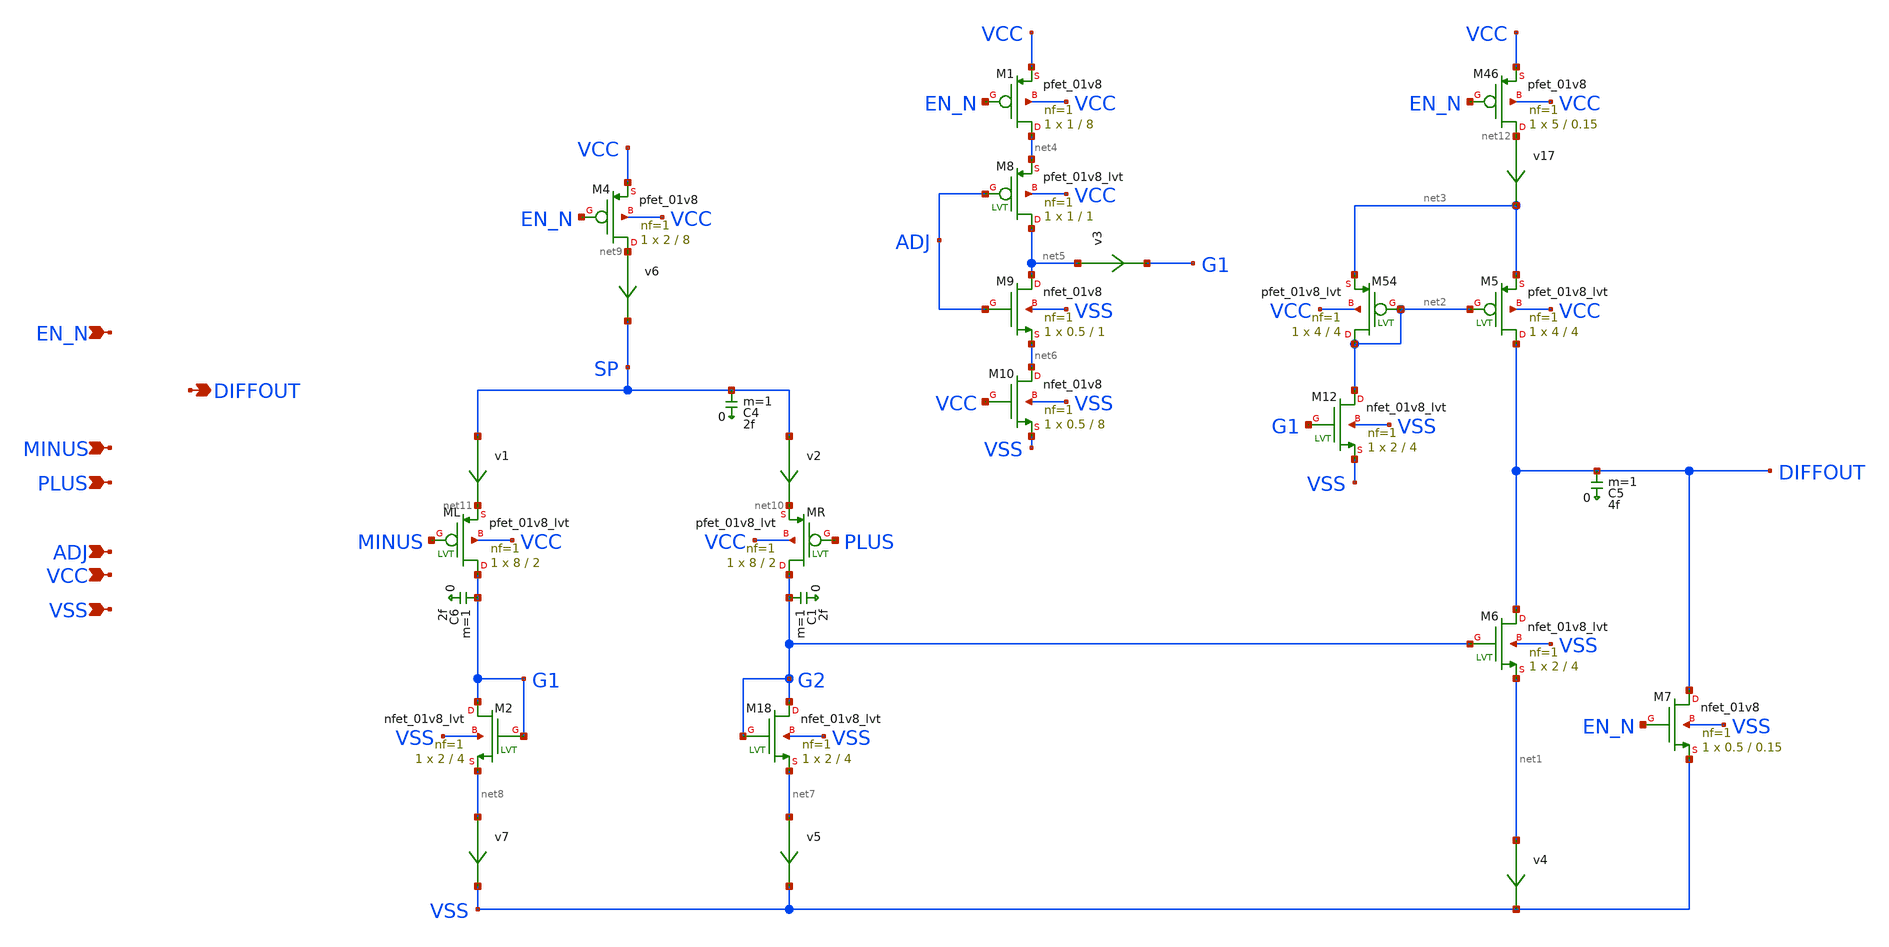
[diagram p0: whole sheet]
** sch_path: sky130A/xschem_libs/sky130_tests/zero_opamp/schematic/zero_opamp.sch
* Copyright 2021 Stefan Frederik Schippers
* Licensed under the Apache License, Version 2.0 (the "License");
* you may not use this file except in compliance with the License.
* You may obtain a copy of the License at
* https://www.apache.org/licenses/LICENSE-2.0
* Unless required by applicable law or agreed to in writing, software
* distributed under the License is distributed on an "AS IS" BASIS,
* WITHOUT WARRANTIES OR CONDITIONS OF ANY KIND, either express or implied.
* See the License for the specific language governing permissions and
* limitations under the License.
**.subckt zero_opamp PLUS MINUS EN_N VSS VCC DIFFOUT ADJ
*.ipin PLUS
*.ipin MINUS
*.ipin EN_N
*.ipin VSS
*.ipin VCC
*.opin DIFFOUT
*.ipin ADJ
C6 G1 0 2f m=1
XM4 net9 EN_N VCC VCC sky130_fd_pr__pfet_01v8 L=8 W=2 nf=1 ad='int((nf+1)/2) * W/nf * 0.29' as='int((nf+2)/2) * W/nf * 0.29'
+ pd='2*int((nf+1)/2) * (W/nf + 0.29)' ps='2*int((nf+2)/2) * (W/nf + 0.29)' nrd='0.29 / W' nrs='0.29 / W'
+ sa=0 sb=0 sd=0 mult=1 m=1
XM18 G2 G2 net7 VSS sky130_fd_pr__nfet_01v8_lvt L=4 W=2 nf=1 ad='int((1 + 1)/2) * 2 / 1 * 0.29' as='int((1 + 2)/2) * 2 / 1 * 0.29'
+ pd='2*int((1 + 1)/2) * (2 / 1 + 0.29)' ps='2*int((1 + 2)/2) * (2 / 1 + 0.29)' nrd='0.29 / 2 ' nrs='0.29 / 2 '
+ sa=0 sb=0 sd=0 mult=1 m=1
XM2 G1 G1 net8 VSS sky130_fd_pr__nfet_01v8_lvt L=4 W=2 nf=1 ad='int((1 + 1)/2) * 2 / 1 * 0.29' as='int((1 + 2)/2) * 2 / 1 * 0.29'
+ pd='2*int((1 + 1)/2) * (2 / 1 + 0.29)' ps='2*int((1 + 2)/2) * (2 / 1 + 0.29)' nrd='0.29 / 2 ' nrs='0.29 / 2 '
+ sa=0 sb=0 sd=0 mult=1 m=1
XMR G2 PLUS net10 VCC sky130_fd_pr__pfet_01v8_lvt L=2 W=8 nf=1 ad='int((1 + 1)/2) * 8 / 1 * 0.29' as='int((1 + 2)/2) * 8 / 1 * 0.29'
+ pd='2*int((1 + 1)/2) * (8 / 1 + 0.29)' ps='2*int((1 + 2)/2) * (8 / 1 + 0.29)' nrd='0.29 / 8 ' nrs='0.29 / 8 '
+ sa=0 sb=0 sd=0 mult=1 m=1
XML G1 MINUS net11 VCC sky130_fd_pr__pfet_01v8_lvt L=2 W=8 nf=1 ad='int((1 + 1)/2) * 8 / 1 * 0.29' as='int((1 + 2)/2) * 8 / 1 * 0.29'
+ pd='2*int((1 + 1)/2) * (8 / 1 + 0.29)' ps='2*int((1 + 2)/2) * (8 / 1 + 0.29)' nrd='0.29 / 8 ' nrs='0.29 / 8 '
+ sa=0 sb=0 sd=0 mult=1 m=1
v1 SP net11 0
.save i(v1)
C4 SP 0 2f m=1
C1 G2 0 2f m=1
C5 DIFFOUT 0 4f m=1
XM6 DIFFOUT G2 net1 VSS sky130_fd_pr__nfet_01v8_lvt L=4 W=2 nf=1 ad='int((1 + 1)/2) * 2 / 1 * 0.29' as='int((1 + 2)/2) * 2 / 1 * 0.29'
+ pd='2*int((1 + 1)/2) * (2 / 1 + 0.29)' ps='2*int((1 + 2)/2) * (2 / 1 + 0.29)' nrd='0.29 / 2 ' nrs='0.29 / 2 '
+ sa=0 sb=0 sd=0 mult=1 m=1
v2 SP net10 0
.save i(v2)
v4 net1 VSS 0
.save i(v4)
v6 net9 SP 0
.save i(v6)
XM7 DIFFOUT EN_N VSS VSS sky130_fd_pr__nfet_01v8 L=0.15 W=0.5 nf=1 ad='int((1 + 1)/2) * 0.5 / 1 * 0.29'
+ as='int((1 + 2)/2) * 0.5 / 1 * 0.29' pd='2*int((1 + 1)/2) * (0.5 / 1 + 0.29)' ps='2*int((1 + 2)/2) * (0.5 / 1 + 0.29)'
+ nrd='0.29 / 0.5 ' nrs='0.29 / 0.5 ' sa=0 sb=0 sd=0 mult=1 m=1
XM46 net12 EN_N VCC VCC sky130_fd_pr__pfet_01v8 L=0.15 W=5 nf=1 ad='int((nf+1)/2) * W/nf * 0.29' as='int((nf+2)/2) * W/nf * 0.29'
+ pd='2*int((nf+1)/2) * (W/nf + 0.29)' ps='2*int((nf+2)/2) * (W/nf + 0.29)' nrd='0.29 / W' nrs='0.29 / W'
+ sa=0 sb=0 sd=0 mult=1 m=1
v17 net12 net3 0
.save i(v17)
XM12 net2 G1 VSS VSS sky130_fd_pr__nfet_01v8_lvt L=4 W=2 nf=1 ad='int((1 + 1)/2) * 2 / 1 * 0.29' as='int((1 + 2)/2) * 2 / 1 * 0.29'
+ pd='2*int((1 + 1)/2) * (2 / 1 + 0.29)' ps='2*int((1 + 2)/2) * (2 / 1 + 0.29)' nrd='0.29 / 2 ' nrs='0.29 / 2 '
+ sa=0 sb=0 sd=0 mult=1 m=1
XM54 net2 net2 net3 VCC sky130_fd_pr__pfet_01v8_lvt L=4 W=4 nf=1 ad='int((1 + 1)/2) * 4 / 1 * 0.29' as='int((1 + 2)/2) * 4 / 1 * 0.29'
+ pd='2*int((1 + 1)/2) * (4 / 1 + 0.29)' ps='2*int((1 + 2)/2) * (4 / 1 + 0.29)' nrd='0.29 / 4 ' nrs='0.29 / 4 '
+ sa=0 sb=0 sd=0 mult=1 m=1
XM5 DIFFOUT net2 net3 VCC sky130_fd_pr__pfet_01v8_lvt L=4 W=4 nf=1 ad='int((1 + 1)/2) * 4 / 1 * 0.29'
+ as='int((1 + 2)/2) * 4 / 1 * 0.29' pd='2*int((1 + 1)/2) * (4 / 1 + 0.29)' ps='2*int((1 + 2)/2) * (4 / 1 + 0.29)'
+ nrd='0.29 / 4 ' nrs='0.29 / 4 ' sa=0 sb=0 sd=0 mult=1 m=1
XM8 net5 ADJ net4 VCC sky130_fd_pr__pfet_01v8_lvt L=1 W=1 nf=1 ad='int((1 + 1)/2) * 1 / 1 * 0.29' as='int((1 + 2)/2) * 1 / 1 * 0.29'
+ pd='2*int((1 + 1)/2) * (1 / 1 + 0.29)' ps='2*int((1 + 2)/2) * (1 / 1 + 0.29)' nrd='0.29 / 1 ' nrs='0.29 / 1 '
+ sa=0 sb=0 sd=0 mult=1 m=1
XM9 net5 ADJ net6 VSS sky130_fd_pr__nfet_01v8 L=1 W=0.5 nf=1 ad='int((1 + 1)/2) * 0.5 / 1 * 0.29' as='int((1 + 2)/2) * 0.5 / 1 * 0.29'
+ pd='2*int((1 + 1)/2) * (0.5 / 1 + 0.29)' ps='2*int((1 + 2)/2) * (0.5 / 1 + 0.29)' nrd='0.29 / 0.5 ' nrs='0.29 / 0.5 '
+ sa=0 sb=0 sd=0 mult=1 m=1
XM10 net6 VCC VSS VSS sky130_fd_pr__nfet_01v8 L=8 W=0.5 nf=1 ad='int((1 + 1)/2) * 0.5 / 1 * 0.29' as='int((1 + 2)/2) * 0.5 / 1 * 0.29'
+ pd='2*int((1 + 1)/2) * (0.5 / 1 + 0.29)' ps='2*int((1 + 2)/2) * (0.5 / 1 + 0.29)' nrd='0.29 / 0.5 ' nrs='0.29 / 0.5 '
+ sa=0 sb=0 sd=0 mult=1 m=1
XM1 net4 EN_N VCC VCC sky130_fd_pr__pfet_01v8 L=8 W=1 nf=1 ad='int((nf+1)/2) * W/nf * 0.29' as='int((nf+2)/2) * W/nf * 0.29'
+ pd='2*int((nf+1)/2) * (W/nf + 0.29)' ps='2*int((nf+2)/2) * (W/nf + 0.29)' nrd='0.29 / W' nrs='0.29 / W'
+ sa=0 sb=0 sd=0 mult=1 m=1
v3 net5 G1 0
.save i(v3)
v5 net7 VSS 0
.save i(v5)
v7 net8 VSS 0
.save i(v7)
**.ends
.end
